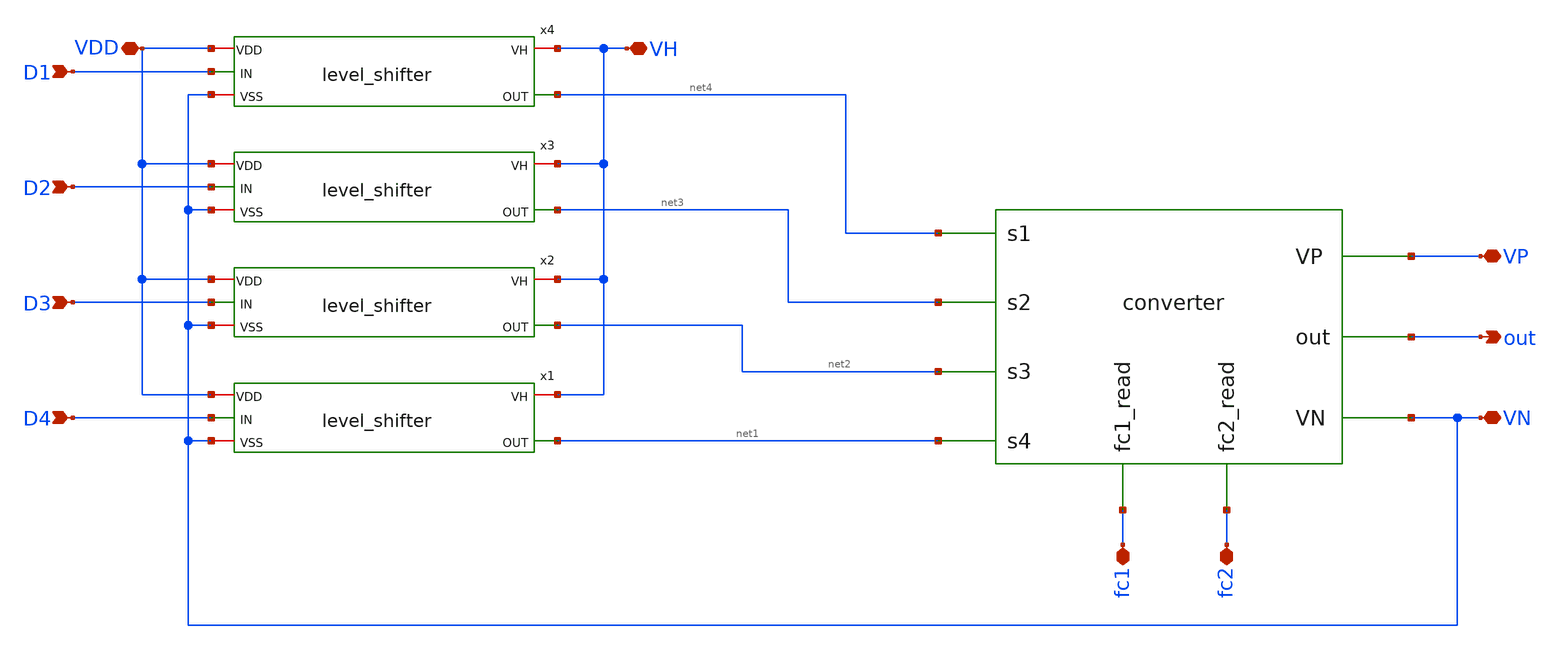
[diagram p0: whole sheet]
** sch_path: ISSCC23/submitted_notebooks/3LFCC/symbols/core.sch
**.subckt core out VP D1 D2 D3 D4 VDD VN VH fc1 fc2
*.opin out
*.iopin VP
*.ipin D1
*.ipin D2
*.ipin D3
*.ipin D4
*.iopin VDD
*.iopin VN
*.iopin VH
*.iopin fc1
*.iopin fc2
X1 net4 net3 net2 net1 out VP VN fc1 fc2 converter
x1 VH VDD net1 D4 VN level_shifter
x2 VH VDD net2 D3 VN level_shifter
x3 VH VDD net3 D2 VN level_shifter
x4 VH VDD net4 D1 VN level_shifter
**.ends
.end
